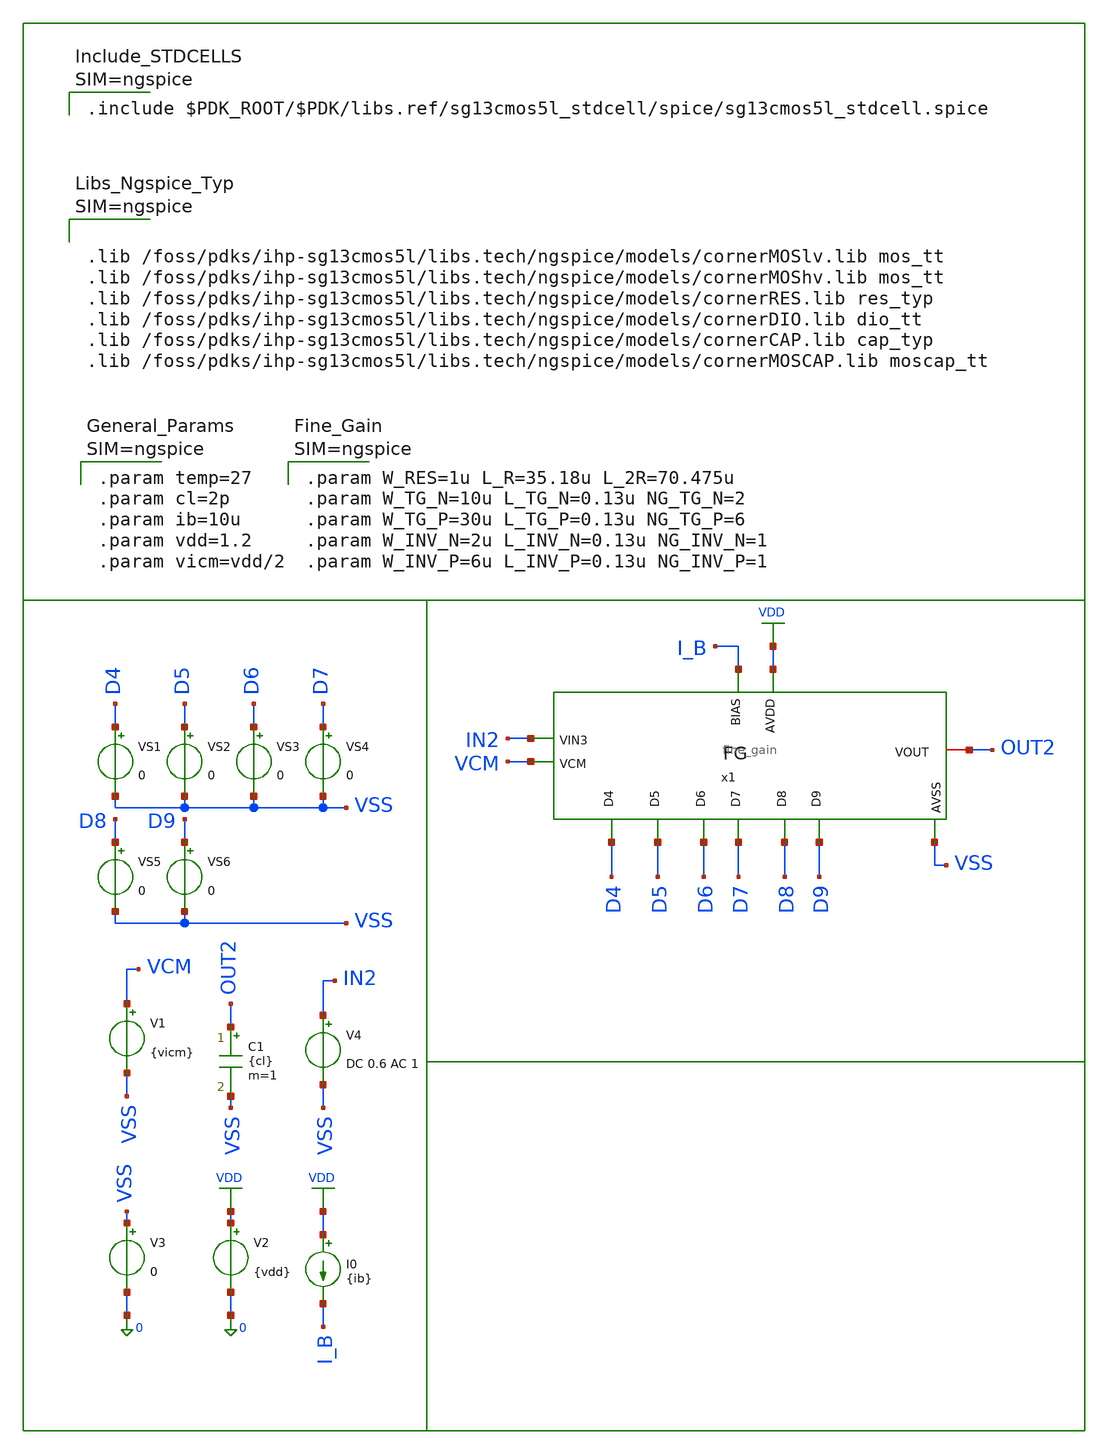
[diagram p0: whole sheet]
** sch_path: designs/archives/fine_gain/tb/tb_fine_gain.sch
**.subckt tb_fine_gain
I0 VDD I_B {ib}
V2 VDD 0 {vdd}
V3 VSS 0 0
V1 VCM VSS {vicm}
C1 OUT2 VSS {cl} m=1
VS1 D4 VSS 0
VS2 D5 VSS 0
VS3 D6 VSS 0
VS4 D7 VSS 0
VS5 D8 VSS 0
VS6 D9 VSS 0
V4 IN2 VSS DC 0.6 AC 1
x1 IN2 I_B OUT2 VCM VDD VSS D4 D5 D6 D7 D8 D9 fine_gain
**** begin user architecture code


.param temp=27
.param cl=2p
.param ib=10u
.param vdd=1.2
.param vicm=vdd/2






.lib /foss/pdks/ihp-sg13cmos5l/libs.tech/ngspice/models/cornerMOSlv.lib mos_tt
.lib /foss/pdks/ihp-sg13cmos5l/libs.tech/ngspice/models/cornerMOShv.lib mos_tt
.lib /foss/pdks/ihp-sg13cmos5l/libs.tech/ngspice/models/cornerRES.lib res_typ
.lib /foss/pdks/ihp-sg13cmos5l/libs.tech/ngspice/models/cornerDIO.lib dio_tt
.lib /foss/pdks/ihp-sg13cmos5l/libs.tech/ngspice/models/cornerCAP.lib cap_typ
.lib /foss/pdks/ihp-sg13cmos5l/libs.tech/ngspice/models/cornerMOSCAP.lib moscap_tt





.control
* ==============================================================================
* FINE-GAIN NETWORK 64-TAP BINARY AUTOMATED CHARACTERIZATION
* ==============================================================================
destroy all
save all
shell mkdir -p result
shell rm -f ./result/tb_fg_network_summary.txt

echo
+ =========================================================================================================== >> ./result/tb_fg_network_summary.txt
echo




.include $PDK_ROOT/$PDK/libs.ref/sg13cmos5l_stdcell/spice/sg13cmos5l_stdcell.spice





.param W_RES=1u L_R=35.18u L_2R=70.475u
.param W_TG_N=10u L_TG_N=0.13u NG_TG_N=2
.param W_TG_P=30u L_TG_P=0.13u NG_TG_P=6
.param W_INV_N=2u L_INV_N=0.13u NG_INV_N=1
.param W_INV_P=6u L_INV_P=0.13u NG_INV_P=1



**** end user architecture code
**.ends
.GLOBAL VDD
.end
